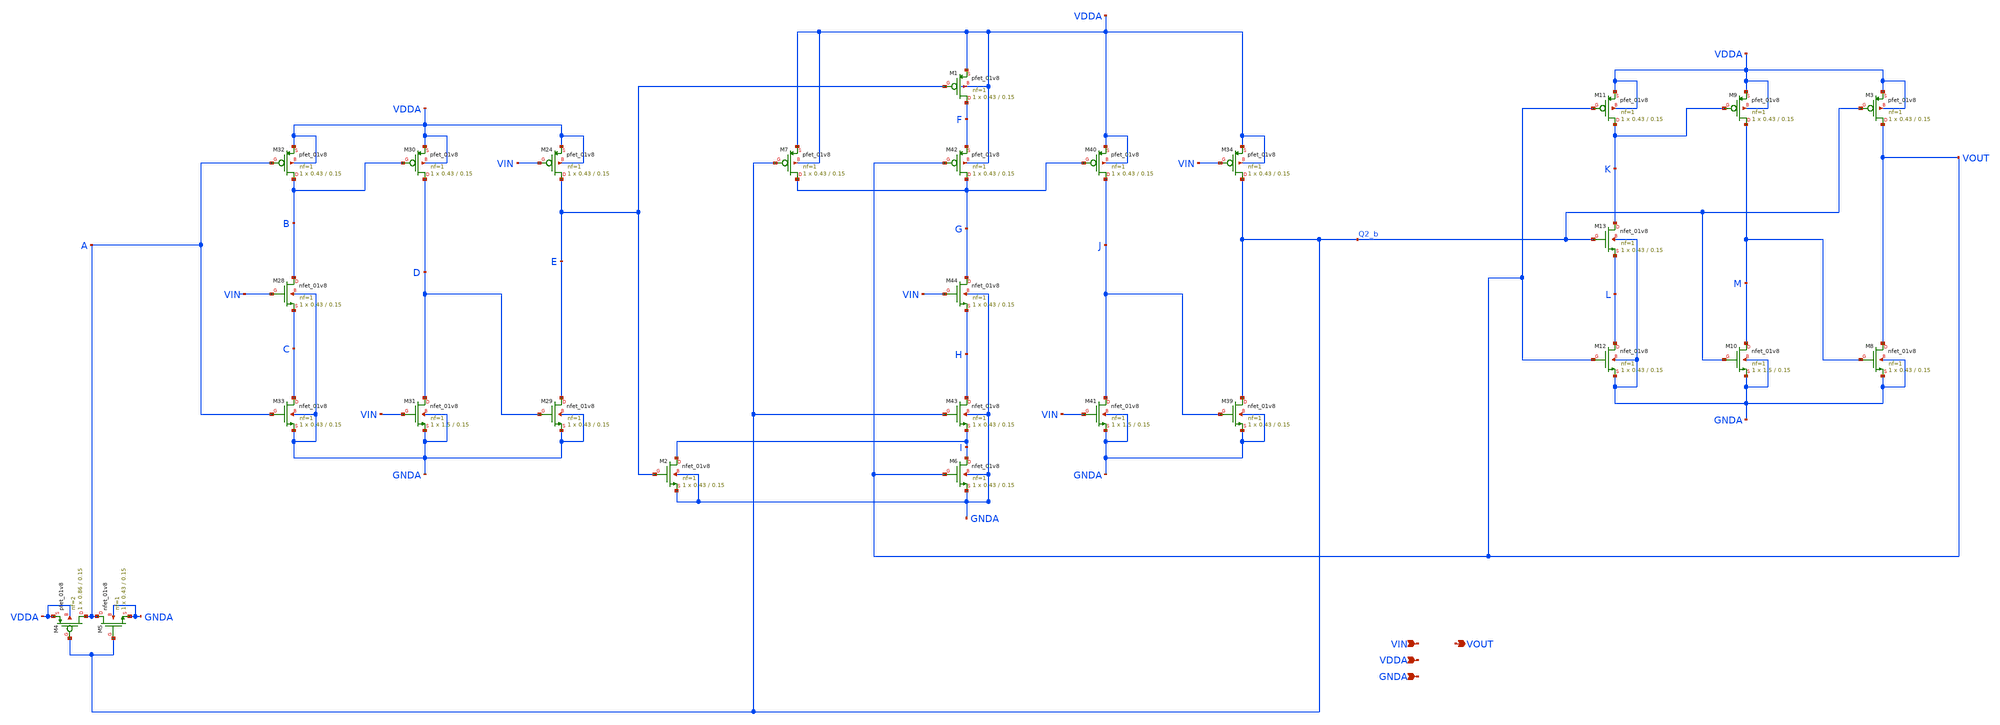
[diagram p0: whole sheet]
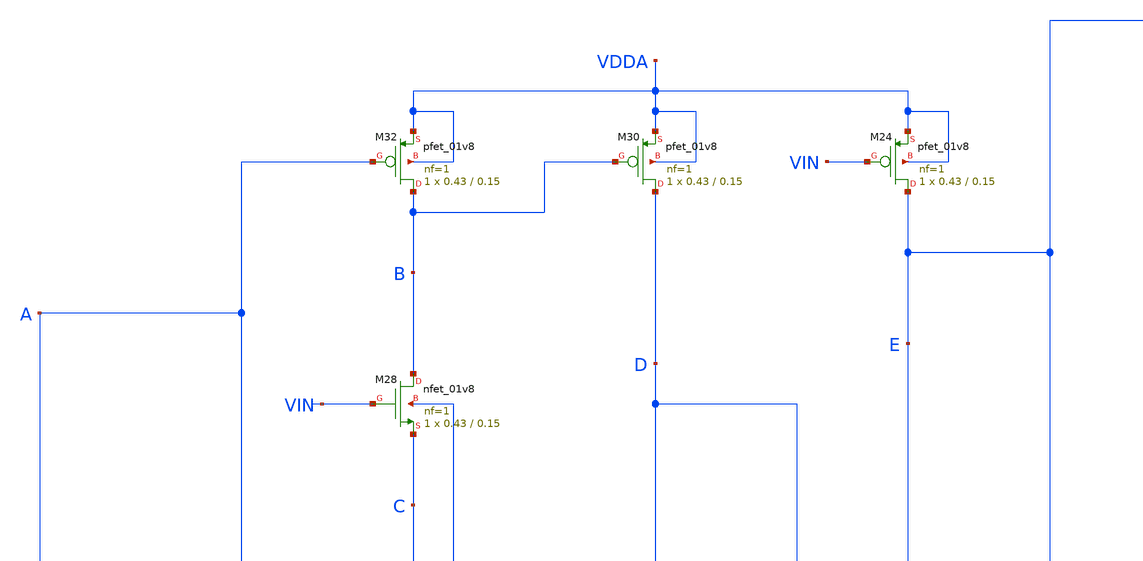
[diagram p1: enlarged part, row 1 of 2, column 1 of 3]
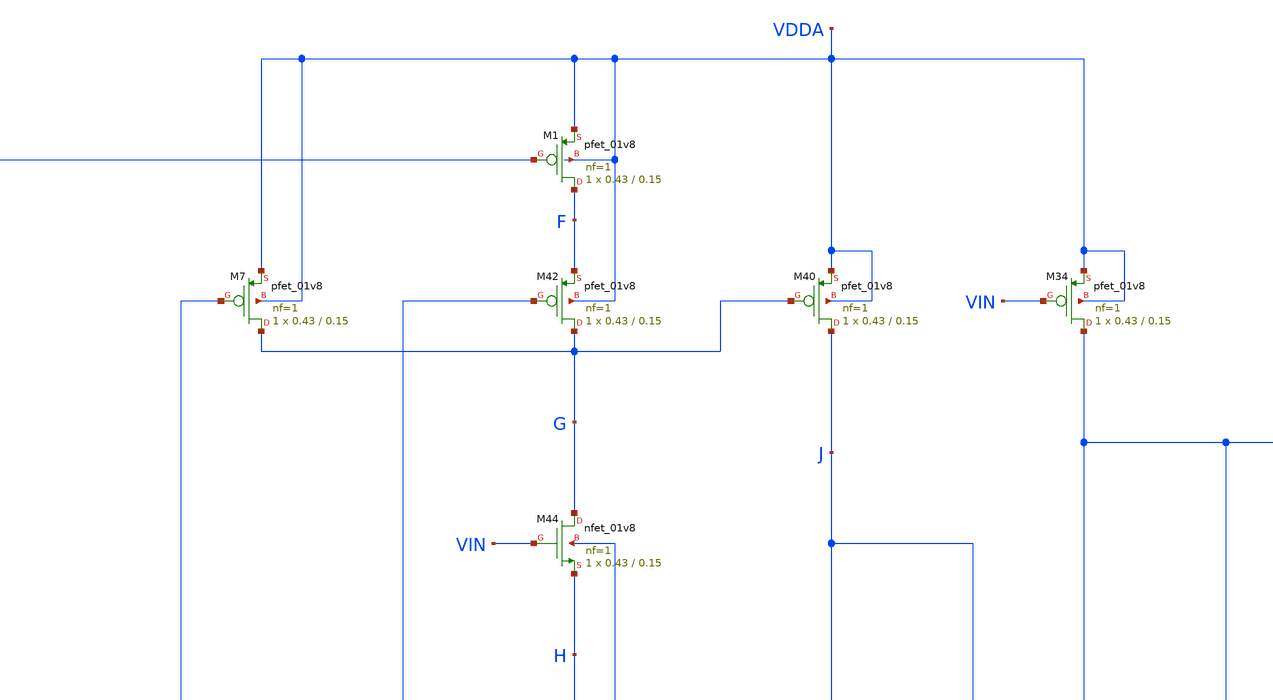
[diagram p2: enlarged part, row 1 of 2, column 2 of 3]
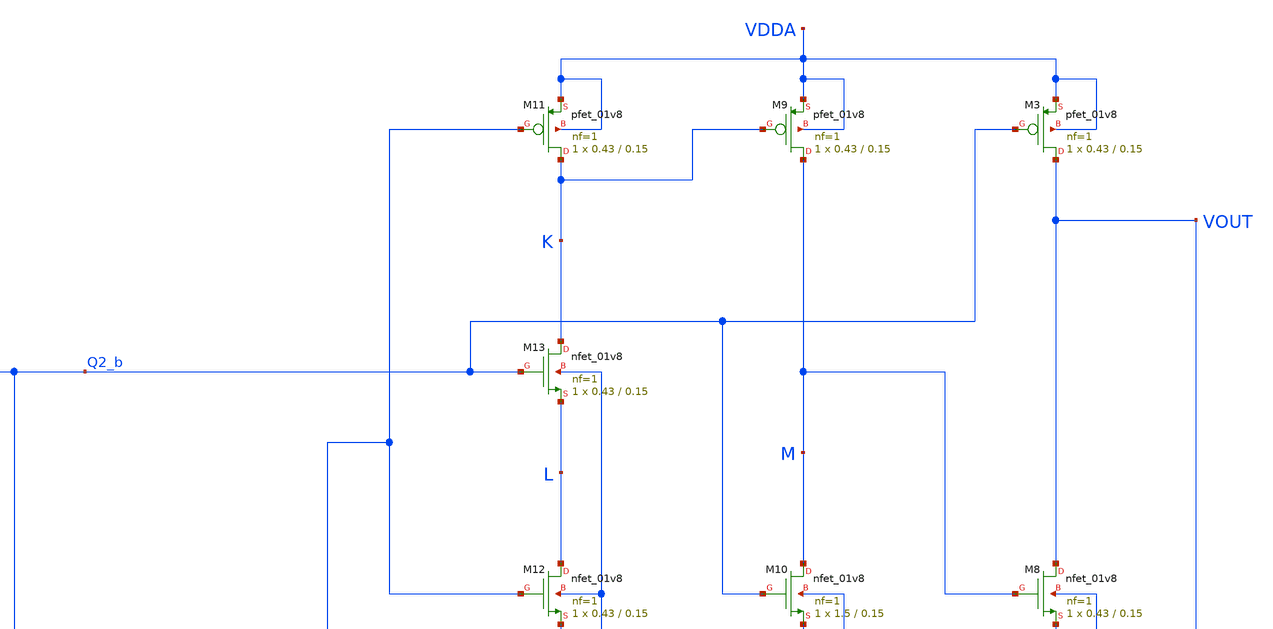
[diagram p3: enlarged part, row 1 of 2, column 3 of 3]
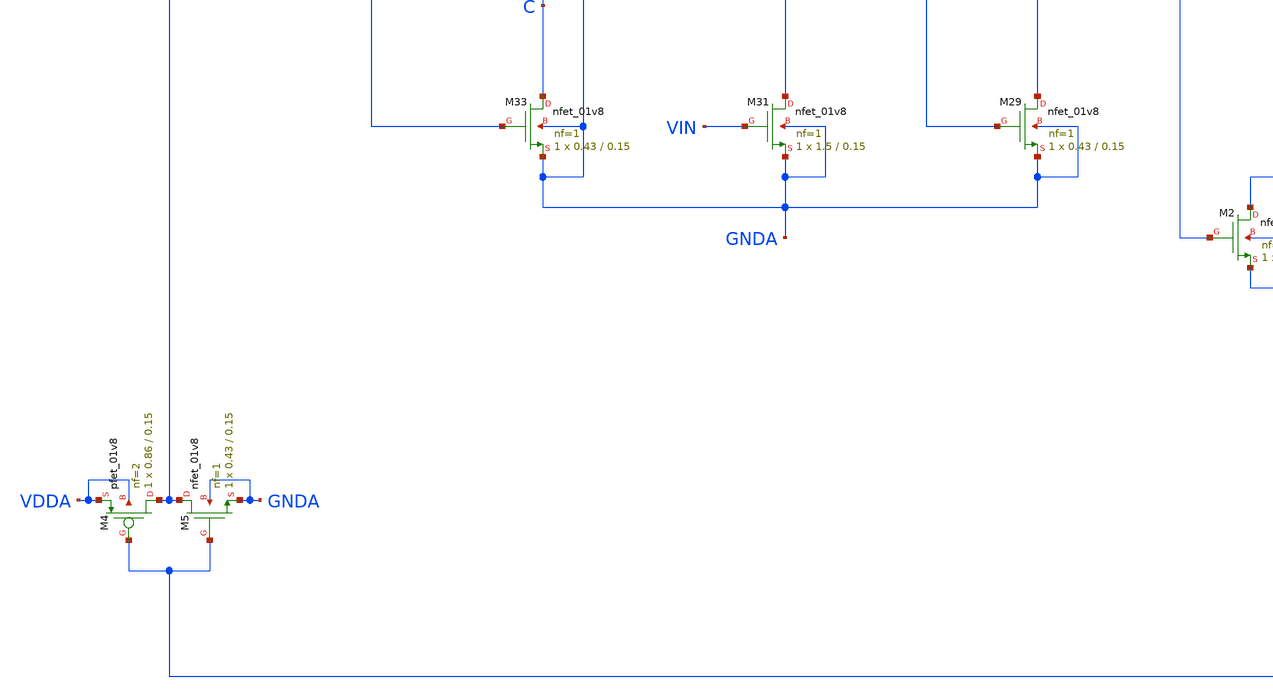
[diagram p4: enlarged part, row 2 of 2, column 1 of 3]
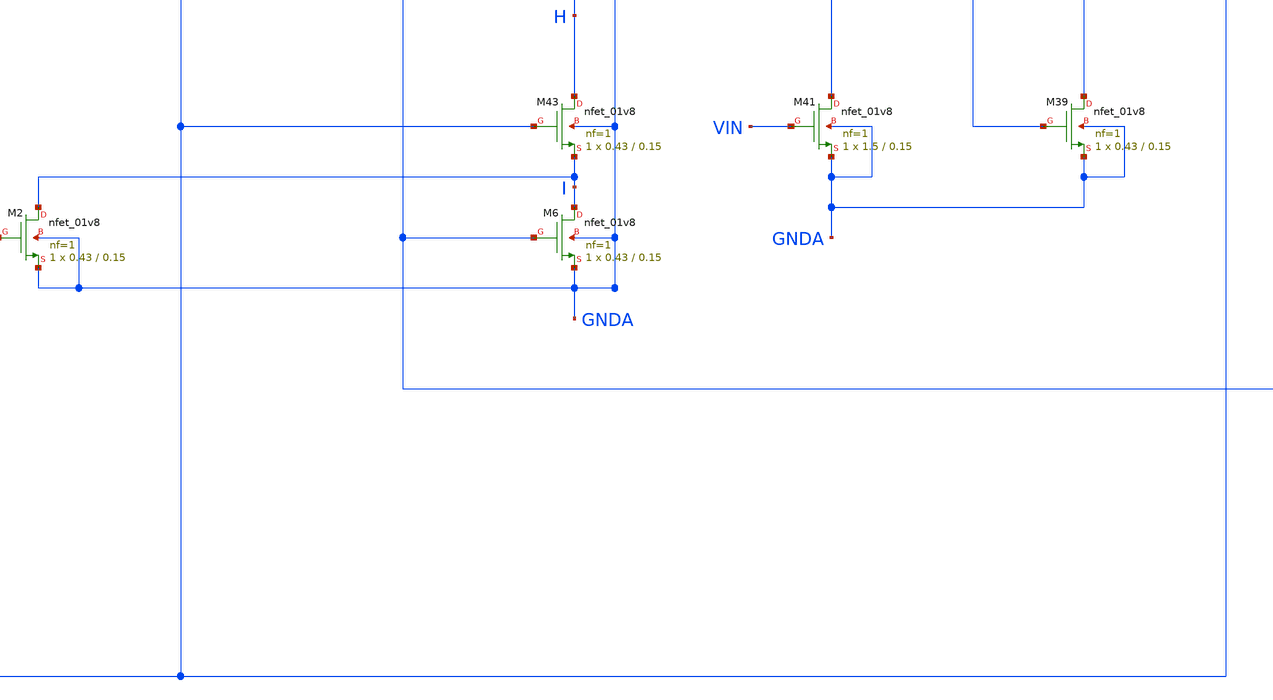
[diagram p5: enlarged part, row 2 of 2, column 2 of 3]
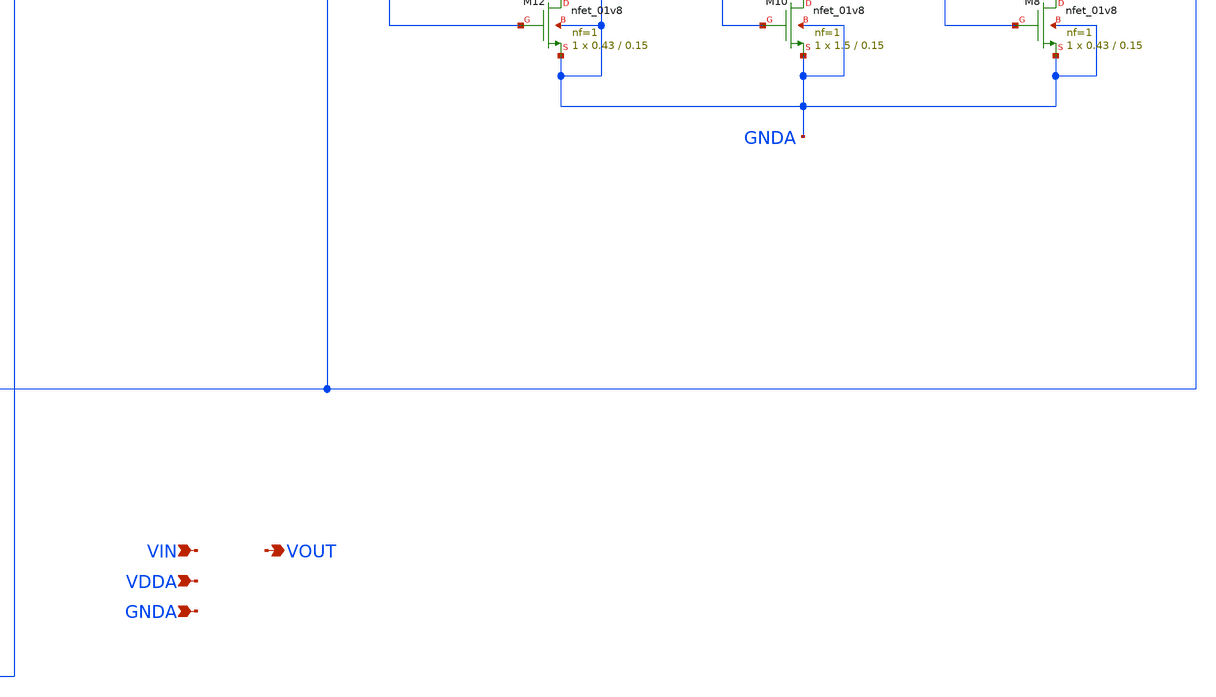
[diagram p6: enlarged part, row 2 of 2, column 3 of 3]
** sch_path: projects/pll/divider/xschem_ngspice/TSPC_FF_ratioed_divide5_2.sch
**.subckt TSPC_FF_ratioed_divide5_2 VIN VOUT VDDA GNDA
*.ipin VIN
*.opin VOUT
*.ipin VDDA
*.ipin GNDA
XM24 E VIN VDDA VDDA sky130_fd_pr__pfet_01v8 L=0.15 W=0.43 nf=1 ad='int((nf+1)/2) * W/nf * 0.29' as='int((nf+2)/2) * W/nf * 0.29'
+ pd='2*int((nf+1)/2) * (W/nf + 0.29)' ps='2*int((nf+2)/2) * (W/nf + 0.29)' nrd='0.29 / W' nrs='0.29 / W'
+ sa=0 sb=0 sd=0 mult=1 m=1
XM29 E D GNDA GNDA sky130_fd_pr__nfet_01v8 L=0.15 W=0.43 nf=1 ad='int((nf+1)/2) * W/nf * 0.29' as='int((nf+2)/2) * W/nf * 0.29'
+ pd='2*int((nf+1)/2) * (W/nf + 0.29)' ps='2*int((nf+2)/2) * (W/nf + 0.29)' nrd='0.29 / W' nrs='0.29 / W'
+ sa=0 sb=0 sd=0 mult=1 m=1
XM30 D B VDDA VDDA sky130_fd_pr__pfet_01v8 L=0.15 W=0.43 nf=1 ad='int((nf+1)/2) * W/nf * 0.29' as='int((nf+2)/2) * W/nf * 0.29'
+ pd='2*int((nf+1)/2) * (W/nf + 0.29)' ps='2*int((nf+2)/2) * (W/nf + 0.29)' nrd='0.29 / W' nrs='0.29 / W'
+ sa=0 sb=0 sd=0 mult=1 m=1
XM31 D VIN GNDA GNDA sky130_fd_pr__nfet_01v8 L=0.15 W=1.5 nf=1 ad='int((nf+1)/2) * W/nf * 0.29' as='int((nf+2)/2) * W/nf * 0.29'
+ pd='2*int((nf+1)/2) * (W/nf + 0.29)' ps='2*int((nf+2)/2) * (W/nf + 0.29)' nrd='0.29 / W' nrs='0.29 / W'
+ sa=0 sb=0 sd=0 mult=1 m=1
XM32 B A VDDA VDDA sky130_fd_pr__pfet_01v8 L=0.15 W=0.43 nf=1 ad='int((nf+1)/2) * W/nf * 0.29' as='int((nf+2)/2) * W/nf * 0.29'
+ pd='2*int((nf+1)/2) * (W/nf + 0.29)' ps='2*int((nf+2)/2) * (W/nf + 0.29)' nrd='0.29 / W' nrs='0.29 / W'
+ sa=0 sb=0 sd=0 mult=1 m=1
XM33 C A GNDA GNDA sky130_fd_pr__nfet_01v8 L=0.15 W=0.43 nf=1 ad='int((nf+1)/2) * W/nf * 0.29' as='int((nf+2)/2) * W/nf * 0.29'
+ pd='2*int((nf+1)/2) * (W/nf + 0.29)' ps='2*int((nf+2)/2) * (W/nf + 0.29)' nrd='0.29 / W' nrs='0.29 / W'
+ sa=0 sb=0 sd=0 mult=1 m=1
XM28 B VIN C GNDA sky130_fd_pr__nfet_01v8 L=0.15 W=0.43 nf=1 ad='int((nf+1)/2) * W/nf * 0.29' as='int((nf+2)/2) * W/nf * 0.29'
+ pd='2*int((nf+1)/2) * (W/nf + 0.29)' ps='2*int((nf+2)/2) * (W/nf + 0.29)' nrd='0.29 / W' nrs='0.29 / W'
+ sa=0 sb=0 sd=0 mult=1 m=1
XM34 Q2_b VIN VDDA VDDA sky130_fd_pr__pfet_01v8 L=0.15 W=0.43 nf=1 ad='int((nf+1)/2) * W/nf * 0.29' as='int((nf+2)/2) * W/nf * 0.29'
+ pd='2*int((nf+1)/2) * (W/nf + 0.29)' ps='2*int((nf+2)/2) * (W/nf + 0.29)' nrd='0.29 / W' nrs='0.29 / W'
+ sa=0 sb=0 sd=0 mult=1 m=1
XM39 Q2_b J GNDA GNDA sky130_fd_pr__nfet_01v8 L=0.15 W=0.43 nf=1 ad='int((nf+1)/2) * W/nf * 0.29' as='int((nf+2)/2) * W/nf * 0.29'
+ pd='2*int((nf+1)/2) * (W/nf + 0.29)' ps='2*int((nf+2)/2) * (W/nf + 0.29)' nrd='0.29 / W' nrs='0.29 / W'
+ sa=0 sb=0 sd=0 mult=1 m=1
XM40 J G VDDA VDDA sky130_fd_pr__pfet_01v8 L=0.15 W=0.43 nf=1 ad='int((nf+1)/2) * W/nf * 0.29' as='int((nf+2)/2) * W/nf * 0.29'
+ pd='2*int((nf+1)/2) * (W/nf + 0.29)' ps='2*int((nf+2)/2) * (W/nf + 0.29)' nrd='0.29 / W' nrs='0.29 / W'
+ sa=0 sb=0 sd=0 mult=1 m=1
XM41 J VIN GNDA GNDA sky130_fd_pr__nfet_01v8 L=0.15 W=1.5 nf=1 ad='int((nf+1)/2) * W/nf * 0.29' as='int((nf+2)/2) * W/nf * 0.29'
+ pd='2*int((nf+1)/2) * (W/nf + 0.29)' ps='2*int((nf+2)/2) * (W/nf + 0.29)' nrd='0.29 / W' nrs='0.29 / W'
+ sa=0 sb=0 sd=0 mult=1 m=1
XM42 G VOUT F VDDA sky130_fd_pr__pfet_01v8 L=0.15 W=0.43 nf=1 ad='int((nf+1)/2) * W/nf * 0.29' as='int((nf+2)/2) * W/nf * 0.29'
+ pd='2*int((nf+1)/2) * (W/nf + 0.29)' ps='2*int((nf+2)/2) * (W/nf + 0.29)' nrd='0.29 / W' nrs='0.29 / W'
+ sa=0 sb=0 sd=0 mult=1 m=1
XM43 H Q2_b I GNDA sky130_fd_pr__nfet_01v8 L=0.15 W=0.43 nf=1 ad='int((nf+1)/2) * W/nf * 0.29' as='int((nf+2)/2) * W/nf * 0.29'
+ pd='2*int((nf+1)/2) * (W/nf + 0.29)' ps='2*int((nf+2)/2) * (W/nf + 0.29)' nrd='0.29 / W' nrs='0.29 / W'
+ sa=0 sb=0 sd=0 mult=1 m=1
XM44 G VIN H GNDA sky130_fd_pr__nfet_01v8 L=0.15 W=0.43 nf=1 ad='int((nf+1)/2) * W/nf * 0.29' as='int((nf+2)/2) * W/nf * 0.29'
+ pd='2*int((nf+1)/2) * (W/nf + 0.29)' ps='2*int((nf+2)/2) * (W/nf + 0.29)' nrd='0.29 / W' nrs='0.29 / W'
+ sa=0 sb=0 sd=0 mult=1 m=1
XM4 A Q2_b VDDA VDDA sky130_fd_pr__pfet_01v8 L=0.15 W=0.86 nf=2 ad='int((nf+1)/2) * W/nf * 0.29' as='int((nf+2)/2) * W/nf * 0.29'
+ pd='2*int((nf+1)/2) * (W/nf + 0.29)' ps='2*int((nf+2)/2) * (W/nf + 0.29)' nrd='0.29 / W' nrs='0.29 / W'
+ sa=0 sb=0 sd=0 mult=1 m=1
XM5 A Q2_b GNDA GNDA sky130_fd_pr__nfet_01v8 L=0.15 W=0.43 nf=1 ad='int((nf+1)/2) * W/nf * 0.29' as='int((nf+2)/2) * W/nf * 0.29'
+ pd='2*int((nf+1)/2) * (W/nf + 0.29)' ps='2*int((nf+2)/2) * (W/nf + 0.29)' nrd='0.29 / W' nrs='0.29 / W'
+ sa=0 sb=0 sd=0 mult=1 m=1
XM6 I VOUT GNDA GNDA sky130_fd_pr__nfet_01v8 L=0.15 W=0.43 nf=1 ad='int((nf+1)/2) * W/nf * 0.29' as='int((nf+2)/2) * W/nf * 0.29'
+ pd='2*int((nf+1)/2) * (W/nf + 0.29)' ps='2*int((nf+2)/2) * (W/nf + 0.29)' nrd='0.29 / W' nrs='0.29 / W'
+ sa=0 sb=0 sd=0 mult=1 m=1
XM7 G Q2_b VDDA VDDA sky130_fd_pr__pfet_01v8 L=0.15 W=0.43 nf=1 ad='int((nf+1)/2) * W/nf * 0.29' as='int((nf+2)/2) * W/nf * 0.29'
+ pd='2*int((nf+1)/2) * (W/nf + 0.29)' ps='2*int((nf+2)/2) * (W/nf + 0.29)' nrd='0.29 / W' nrs='0.29 / W'
+ sa=0 sb=0 sd=0 mult=1 m=1
XM1 F E VDDA VDDA sky130_fd_pr__pfet_01v8 L=0.15 W=0.43 nf=1 ad='int((nf+1)/2) * W/nf * 0.29' as='int((nf+2)/2) * W/nf * 0.29'
+ pd='2*int((nf+1)/2) * (W/nf + 0.29)' ps='2*int((nf+2)/2) * (W/nf + 0.29)' nrd='0.29 / W' nrs='0.29 / W'
+ sa=0 sb=0 sd=0 mult=1 m=1
XM2 I E GNDA GNDA sky130_fd_pr__nfet_01v8 L=0.15 W=0.43 nf=1 ad='int((nf+1)/2) * W/nf * 0.29' as='int((nf+2)/2) * W/nf * 0.29'
+ pd='2*int((nf+1)/2) * (W/nf + 0.29)' ps='2*int((nf+2)/2) * (W/nf + 0.29)' nrd='0.29 / W' nrs='0.29 / W'
+ sa=0 sb=0 sd=0 mult=1 m=1
XM3 VOUT Q2_b VDDA VDDA sky130_fd_pr__pfet_01v8 L=0.15 W=0.43 nf=1 ad='int((nf+1)/2) * W/nf * 0.29' as='int((nf+2)/2) * W/nf * 0.29'
+ pd='2*int((nf+1)/2) * (W/nf + 0.29)' ps='2*int((nf+2)/2) * (W/nf + 0.29)' nrd='0.29 / W' nrs='0.29 / W'
+ sa=0 sb=0 sd=0 mult=1 m=1
XM8 VOUT M GNDA GNDA sky130_fd_pr__nfet_01v8 L=0.15 W=0.43 nf=1 ad='int((nf+1)/2) * W/nf * 0.29' as='int((nf+2)/2) * W/nf * 0.29'
+ pd='2*int((nf+1)/2) * (W/nf + 0.29)' ps='2*int((nf+2)/2) * (W/nf + 0.29)' nrd='0.29 / W' nrs='0.29 / W'
+ sa=0 sb=0 sd=0 mult=1 m=1
XM9 M K VDDA VDDA sky130_fd_pr__pfet_01v8 L=0.15 W=0.43 nf=1 ad='int((nf+1)/2) * W/nf * 0.29' as='int((nf+2)/2) * W/nf * 0.29'
+ pd='2*int((nf+1)/2) * (W/nf + 0.29)' ps='2*int((nf+2)/2) * (W/nf + 0.29)' nrd='0.29 / W' nrs='0.29 / W'
+ sa=0 sb=0 sd=0 mult=1 m=1
XM10 M Q2_b GNDA GNDA sky130_fd_pr__nfet_01v8 L=0.15 W=1.5 nf=1 ad='int((nf+1)/2) * W/nf * 0.29' as='int((nf+2)/2) * W/nf * 0.29'
+ pd='2*int((nf+1)/2) * (W/nf + 0.29)' ps='2*int((nf+2)/2) * (W/nf + 0.29)' nrd='0.29 / W' nrs='0.29 / W'
+ sa=0 sb=0 sd=0 mult=1 m=1
XM11 K VOUT VDDA VDDA sky130_fd_pr__pfet_01v8 L=0.15 W=0.43 nf=1 ad='int((nf+1)/2) * W/nf * 0.29' as='int((nf+2)/2) * W/nf * 0.29'
+ pd='2*int((nf+1)/2) * (W/nf + 0.29)' ps='2*int((nf+2)/2) * (W/nf + 0.29)' nrd='0.29 / W' nrs='0.29 / W'
+ sa=0 sb=0 sd=0 mult=1 m=1
XM12 L VOUT GNDA GNDA sky130_fd_pr__nfet_01v8 L=0.15 W=0.43 nf=1 ad='int((nf+1)/2) * W/nf * 0.29' as='int((nf+2)/2) * W/nf * 0.29'
+ pd='2*int((nf+1)/2) * (W/nf + 0.29)' ps='2*int((nf+2)/2) * (W/nf + 0.29)' nrd='0.29 / W' nrs='0.29 / W'
+ sa=0 sb=0 sd=0 mult=1 m=1
XM13 K Q2_b L GNDA sky130_fd_pr__nfet_01v8 L=0.15 W=0.43 nf=1 ad='int((nf+1)/2) * W/nf * 0.29' as='int((nf+2)/2) * W/nf * 0.29'
+ pd='2*int((nf+1)/2) * (W/nf + 0.29)' ps='2*int((nf+2)/2) * (W/nf + 0.29)' nrd='0.29 / W' nrs='0.29 / W'
+ sa=0 sb=0 sd=0 mult=1 m=1
**.ends
.end
